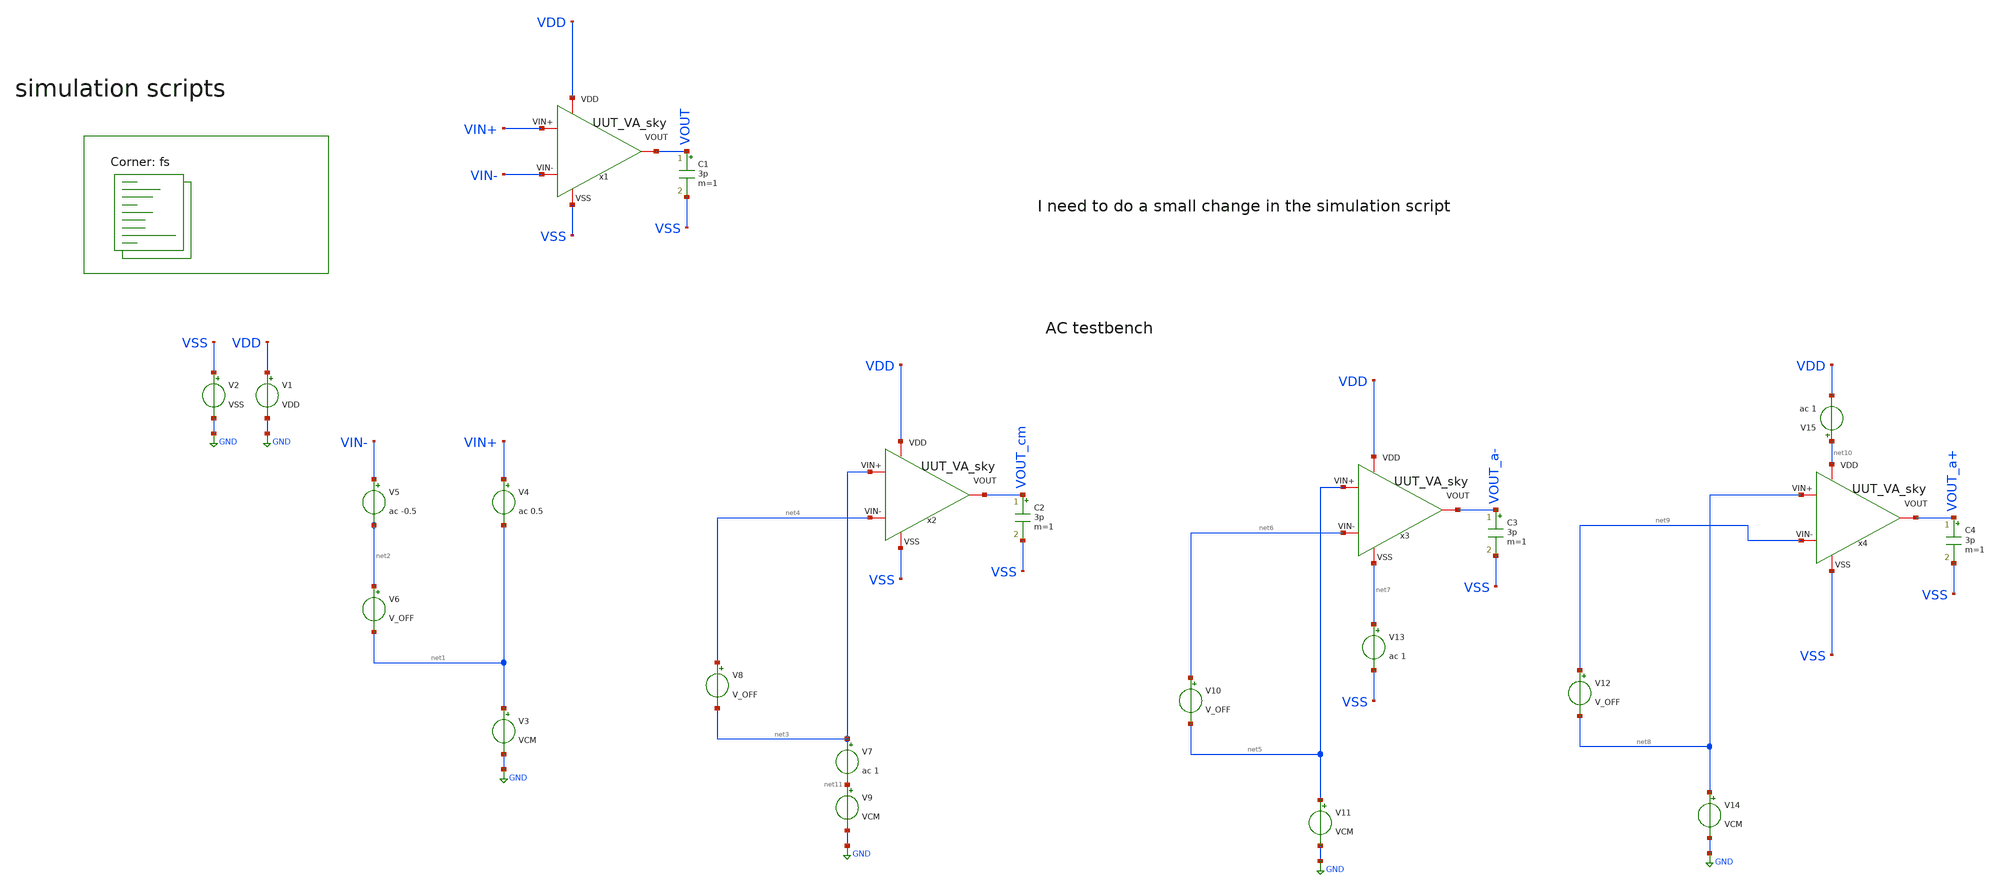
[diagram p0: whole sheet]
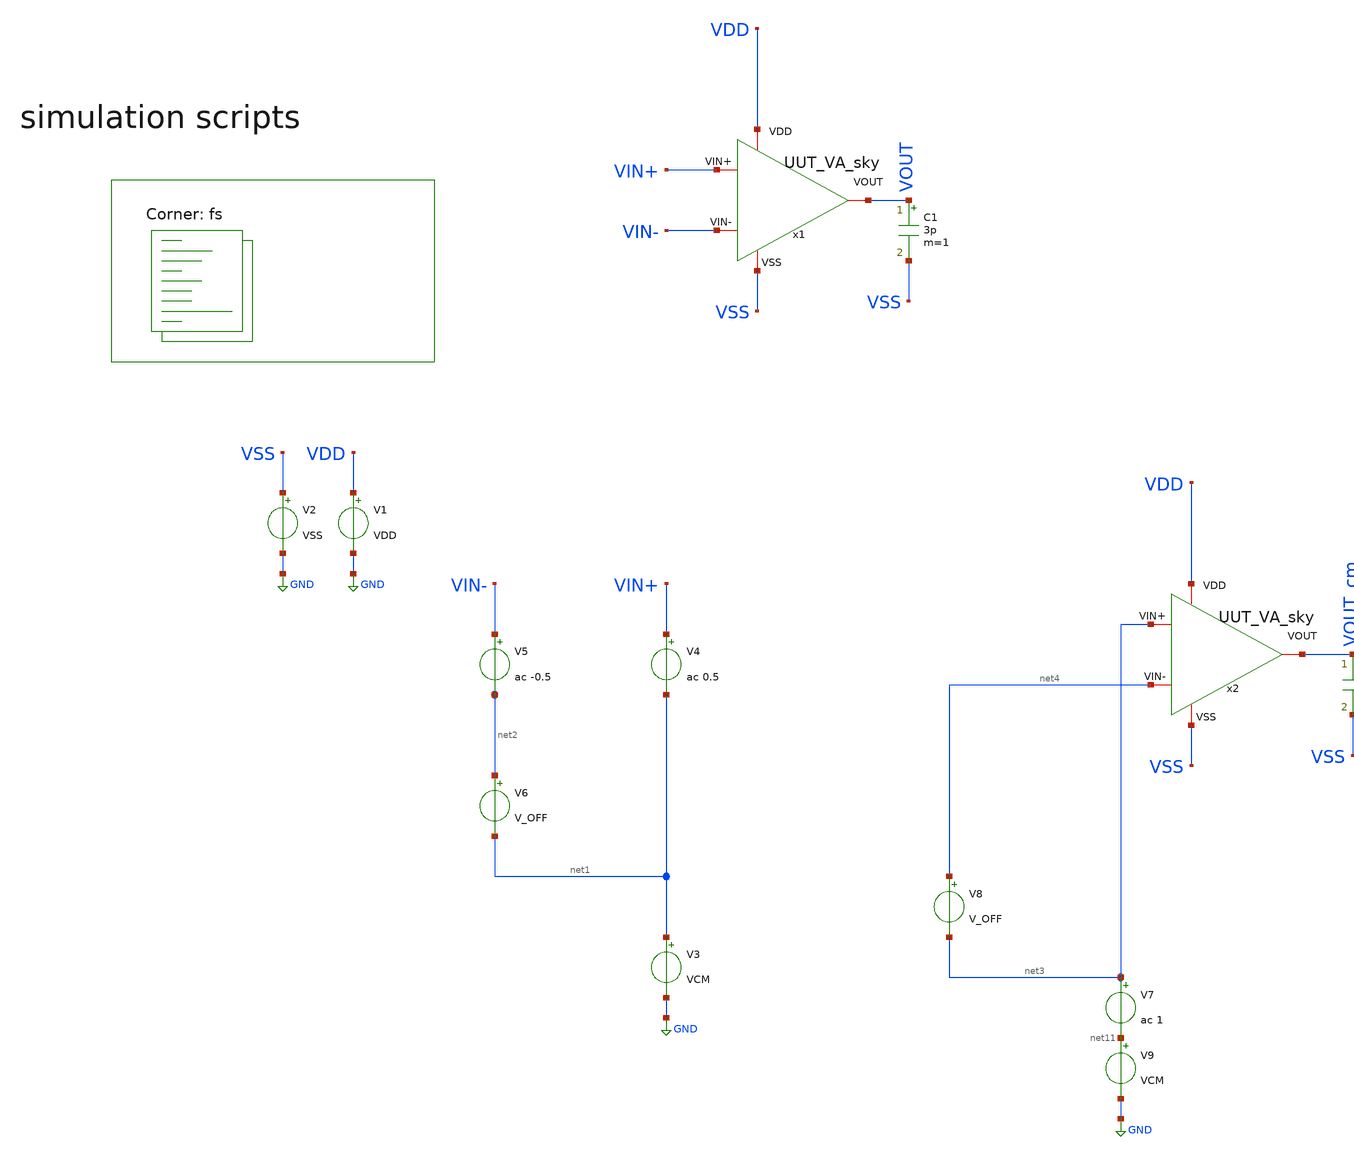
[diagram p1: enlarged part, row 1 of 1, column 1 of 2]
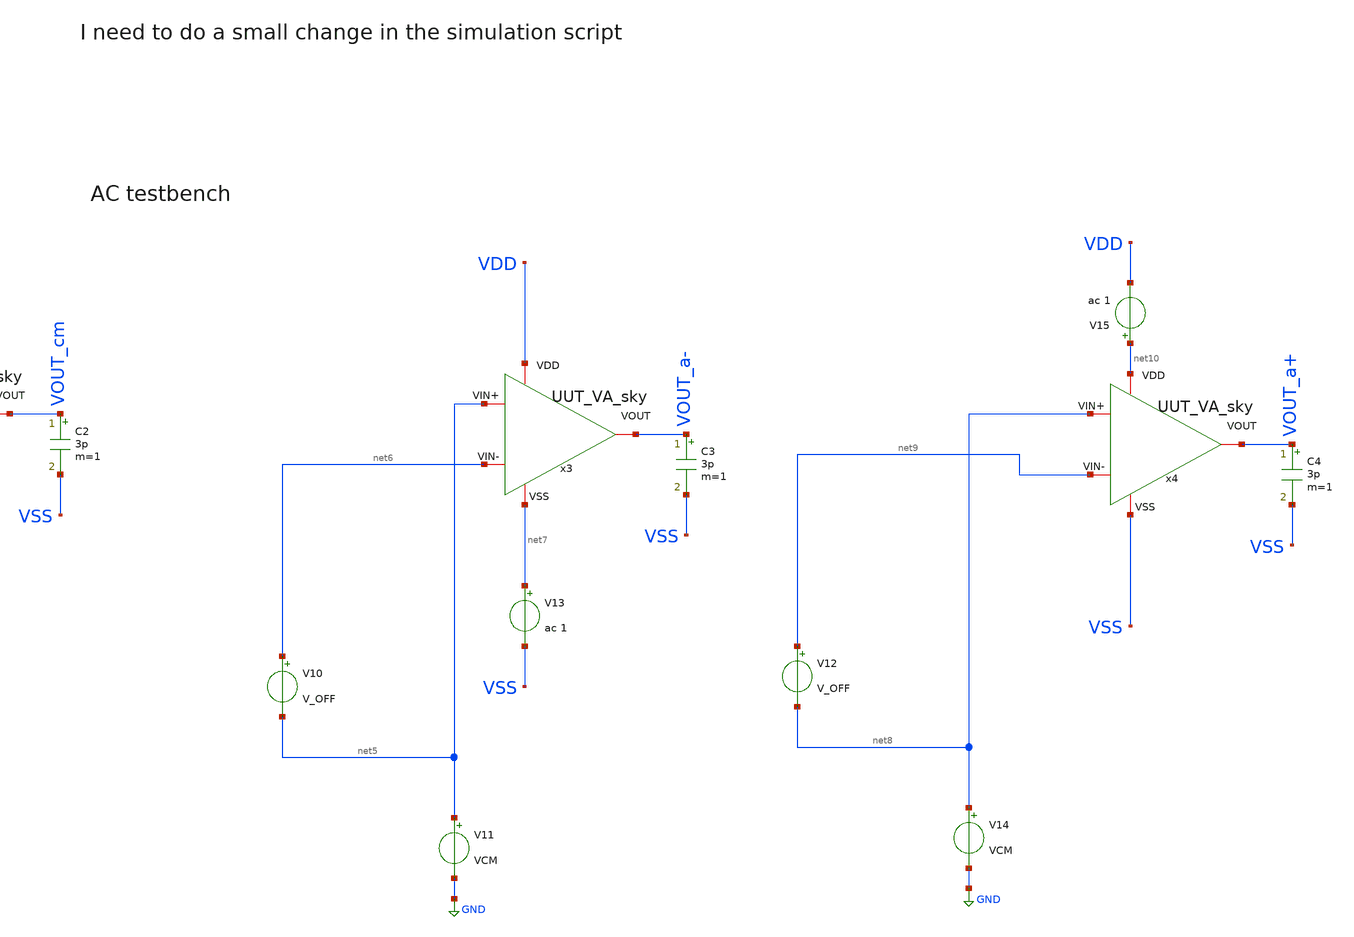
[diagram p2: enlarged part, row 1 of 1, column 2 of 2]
** sch_path: Learning/single_ended_amplifiers/Design_and_Analysis_of_Two-Stage_CMOS_Operational_Amplifier_for_Fluorescence_Signal_Processing_sky130_5V/amplifier_design/OTA_AC_TB.sch
**.subckt OTA_AC_TB
V1 VDD GND VDD
V2 VSS GND VSS
V4 VIN+ net1 ac 0.5
V6 net2 net1 V_OFF
V3 net1 GND VCM
C1 VOUT VSS 3p m=1
V8 net4 net3 V_OFF
V9 net11 GND VCM
V7 net3 net11 ac 1
V10 net6 net5 V_OFF
V11 net5 GND VCM
V13 net7 VSS ac 1
V12 net9 net8 V_OFF
V14 net8 GND VCM
V15 net10 VDD ac 1
x1 VDD VSS VIN- VIN+ VOUT UUT_VA_sky
x2 VDD VSS net4 net3 VOUT_cm UUT_VA_sky
x3 VDD net7 net6 net5 VOUT_a- UUT_VA_sky
x4 net10 VSS net9 net8 VOUT_a+ UUT_VA_sky
V5 VIN- net2 ac -0.5
C2 VOUT_cm VSS 3p m=1
C3 VOUT_a- VSS 3p m=1
C4 VOUT_a+ VSS 3p m=1
**** begin user architecture code
.lib $::SKYWATER_MODELS/sky130.lib.spice fs

.Temp 27
.param VDD = 5
.param VSS = 0
.param CL = 3p
.param V_OFF = -806.71u
.param VCM=2.5


.control

	save all
	ac dec 100 1 10G
	plot db(v(VOUT))
	plot db(v(VOUT_CM))
	plot db(v(VOUT_A-))
	plot db(v(VOUT_A+))
	wrdata VIN_sweep_AC.csv db(v(VOUT)) phase(v(VOUT)) db(v(VOUT_CM)) db(v(VOUT_A-)) db(v(VOUT_A+))
.endc




**** end user architecture code
**.ends

* expanding   symbol:  Sky130A/UUT_sky/UUT_VA_sky.sym # of pins=5
** sym_path: my_ip/LIB/Sky130A/UUT_sky/UUT_VA_sky.sym
** sch_path: my_ip/LIB/Sky130A/UUT_sky/UUT_VA_sky.sch
.subckt UUT_VA_sky VDD VSS VIN- VIN+ VOUT
*.iopin VDD
*.iopin VSS
*.iopin VIN-
*.iopin VIN+
*.iopin VOUT
x1 VDD VSS VIN+ VIN- VOUT amplifier
.ends


* expanding   symbol:
*+  Sky130A/Learning/Design_of_Two-Stage_CMOS_Operational_Amplifier_for_Fluorescence_Signal_Processing_5V/amplifier.sym # of pins=5
** sym_path: my_ip/LIB/Sky130A/Learning/Design_of_Two-Stage_CMOS_Operational_Amplifier_for_Fluorescence_Signal_Processing_5V/amplifier.sym
** sch_path: my_ip/LIB/Sky130A/Learning/Design_of_Two-Stage_CMOS_Operational_Amplifier_for_Fluorescence_Signal_Processing_5V/amplifier.sch
.subckt amplifier VDD VSS Vin+ Vin- VOUT
*.iopin VDD
*.iopin VSS
*.iopin Vin+
*.iopin Vin-
*.iopin VOUT
XR2 VSS net2 VSS sky130_fd_pr__res_high_po_0p35 L=20.4 mult=1 m=1
XM7 net1 net1 VSS VSS sky130_fd_pr__nfet_g5v0d10v5 L=3.2 W='1 * 2 ' nf=2 ad='int((nf+1)/2) * W / nf * 0.29'
+ as='int((nf+2)/2) * W / nf * 0.29' pd='2*int((nf+1)/2) * (W / nf + 0.29)' ps='2*int((nf+2)/2) * (W / nf + 0.29)'
+ nrd='0.29 / W ' nrs='0.29 / W ' sa=0 sb=0 sd=0 mult=2 m=2
XM8 net3 net1 net2 VSS sky130_fd_pr__nfet_g5v0d10v5 L=3.2 W='1 * 8 ' nf=8 ad='int((nf+1)/2) * W / nf * 0.29'
+ as='int((nf+2)/2) * W / nf * 0.29' pd='2*int((nf+1)/2) * (W / nf + 0.29)' ps='2*int((nf+2)/2) * (W / nf + 0.29)'
+ nrd='0.29 / W ' nrs='0.29 / W ' sa=0 sb=0 sd=0 mult=2 m=2
XM9 VB1 VB2 net3 VSS sky130_fd_pr__nfet_g5v0d10v5 L=2 W='1 * 2 ' nf=2 ad='int((nf+1)/2) * W / nf * 0.29'
+ as='int((nf+2)/2) * W / nf * 0.29' pd='2*int((nf+1)/2) * (W / nf + 0.29)' ps='2*int((nf+2)/2) * (W / nf + 0.29)'
+ nrd='0.29 / W ' nrs='0.29 / W ' sa=0 sb=0 sd=0 mult=2 m=2
XM10 VB2 VB2 net1 VSS sky130_fd_pr__nfet_g5v0d10v5 L=2 W='1 * 2 ' nf=2 ad='int((nf+1)/2) * W / nf * 0.29'
+ as='int((nf+2)/2) * W / nf * 0.29' pd='2*int((nf+1)/2) * (W / nf + 0.29)' ps='2*int((nf+2)/2) * (W / nf + 0.29)'
+ nrd='0.29 / W ' nrs='0.29 / W ' sa=0 sb=0 sd=0 mult=2 m=2
XM2 net6 Vin- net4 net4 sky130_fd_pr__pfet_g5v0d10v5 L=1 W='4.5 * 2 ' nf=2 ad='int((2 + 1)/2) * 4.5 * 0.29'
+ as='int((2 + 2)/2) * 4.5 * 0.29' pd='2*int((2 + 1)/2) * (4.5 + 0.29)' ps='2*int((2 + 2)/2) * (4.5 + 0.29)'
+ nrd='0.29 / 4.5 / 2 ' nrs='0.29 / 4.5 / 2 ' sa=0 sb=0 sd=0 mult=4 m=4
XM3 net5 Vin+ net4 net4 sky130_fd_pr__pfet_g5v0d10v5 L=1 W='4.5 * 2 ' nf=2 ad='int((2 + 1)/2) * 4.5 * 0.29'
+ as='int((2 + 2)/2) * 4.5 * 0.29' pd='2*int((2 + 1)/2) * (4.5 + 0.29)' ps='2*int((2 + 2)/2) * (4.5 + 0.29)'
+ nrd='0.29 / 4.5 / 2 ' nrs='0.29 / 4.5 / 2 ' sa=0 sb=0 sd=0 mult=4 m=4
XM4 net5 net6 VSS VSS sky130_fd_pr__nfet_g5v0d10v5 L=2 W='1.5 * 2 ' nf=2 ad='int((nf+1)/2) * W / nf * 0.29'
+ as='int((nf+2)/2) * W / nf * 0.29' pd='2*int((nf+1)/2) * (W / nf + 0.29)' ps='2*int((nf+2)/2) * (W / nf + 0.29)'
+ nrd='0.29 / W ' nrs='0.29 / W ' sa=0 sb=0 sd=0 mult=2 m=2
XM11 net6 net6 VSS VSS sky130_fd_pr__nfet_g5v0d10v5 L=2 W='1.5 * 2 ' nf=2 ad='int((nf+1)/2) * W / nf * 0.29'
+ as='int((nf+2)/2) * W / nf * 0.29' pd='2*int((nf+1)/2) * (W / nf + 0.29)' ps='2*int((nf+2)/2) * (W / nf + 0.29)'
+ nrd='0.29 / W ' nrs='0.29 / W ' sa=0 sb=0 sd=0 mult=2 m=2
XM13 VOUT net5 VSS VSS sky130_fd_pr__nfet_g5v0d10v5 L=1 W='4 * 2 ' nf=2 ad='int((nf+1)/2) * W / nf * 0.29'
+ as='int((nf+2)/2) * W / nf * 0.29' pd='2*int((nf+1)/2) * (W / nf + 0.29)' ps='2*int((nf+2)/2) * (W / nf + 0.29)'
+ nrd='0.29 / W ' nrs='0.29 / W ' sa=0 sb=0 sd=0 mult=2 m=2
XM14 net7 VB2 net5 VSS sky130_fd_pr__nfet_g5v0d10v5 L=2 W='1.4 * 1 ' nf=1 ad='int((nf+1)/2) * W / nf * 0.29'
+ as='int((nf+2)/2) * W / nf * 0.29' pd='2*int((nf+1)/2) * (W / nf + 0.29)' ps='2*int((nf+2)/2) * (W / nf + 0.29)'
+ nrd='0.29 / W ' nrs='0.29 / W ' sa=0 sb=0 sd=0 mult=2 m=2
XC1 VOUT net7 sky130_fd_pr__cap_mim_m3_1 W=8 L=8 MF=4 m=4
XM1 VB2 VB1 VDD VDD sky130_fd_pr__pfet_g5v0d10v5 L=2.2 W='1 * 2 ' nf=2 ad='int((2 + 1)/2) * 1 * 0.29'
+ as='int((2 + 2)/2) * 1 * 0.29' pd='2*int((2 + 1)/2) * (1 + 0.29)' ps='2*int((2 + 2)/2) * (1 + 0.29)'
+ nrd='0.29 / 1 / 2 ' nrs='0.29 / 1 / 2 ' sa=0 sb=0 sd=0 mult=2 m=2
XM5 VB1 VB1 VDD VDD sky130_fd_pr__pfet_g5v0d10v5 L=2.2 W='1 * 2 ' nf=2 ad='int((2 + 1)/2) * 1 * 0.29'
+ as='int((2 + 2)/2) * 1 * 0.29' pd='2*int((2 + 1)/2) * (1 + 0.29)' ps='2*int((2 + 2)/2) * (1 + 0.29)'
+ nrd='0.29 / 1 / 2 ' nrs='0.29 / 1 / 2 ' sa=0 sb=0 sd=0 mult=2 m=2
XM6 net4 VB1 VDD VDD sky130_fd_pr__pfet_g5v0d10v5 L=2.2 W='1 * 2 ' nf=2 ad='int((2 + 1)/2) * 1 * 0.29'
+ as='int((2 + 2)/2) * 1 * 0.29' pd='2*int((2 + 1)/2) * (1 + 0.29)' ps='2*int((2 + 2)/2) * (1 + 0.29)'
+ nrd='0.29 / 1 / 2 ' nrs='0.29 / 1 / 2 ' sa=0 sb=0 sd=0 mult=8 m=8
XM12 VOUT VB1 VDD VDD sky130_fd_pr__pfet_g5v0d10v5 L=2.2 W='1 * 2 ' nf=2 ad='int((2 + 1)/2) * 1 * 0.29'
+ as='int((2 + 2)/2) * 1 * 0.29' pd='2*int((2 + 1)/2) * (1 + 0.29)' ps='2*int((2 + 2)/2) * (1 + 0.29)'
+ nrd='0.29 / 1 / 2 ' nrs='0.29 / 1 / 2 ' sa=0 sb=0 sd=0 mult=16 m=16
.ends

.GLOBAL GND
.end
